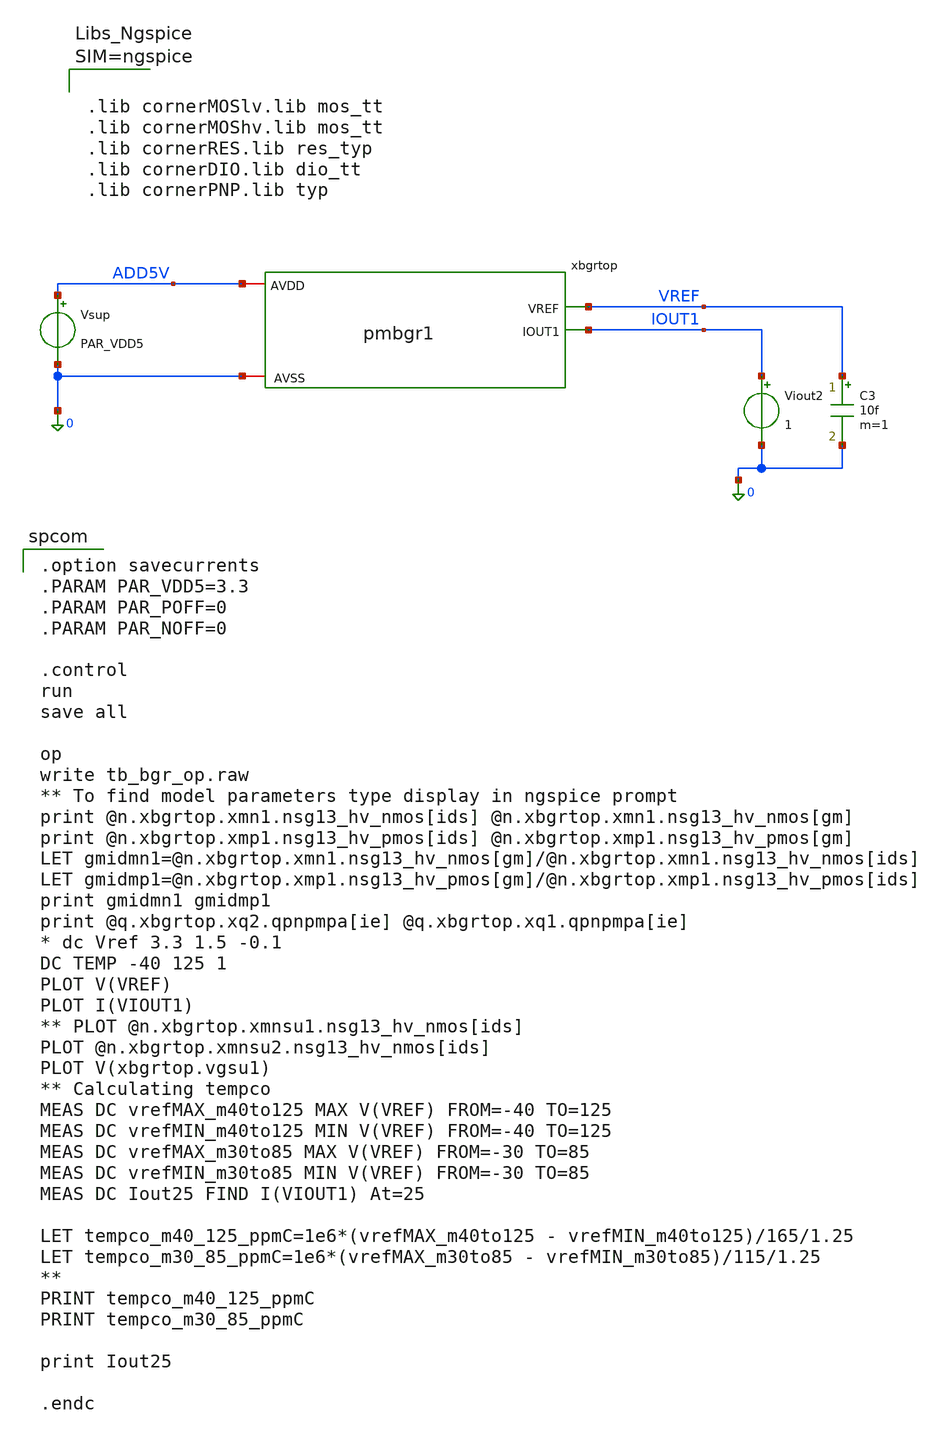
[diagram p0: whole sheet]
** sch_path: xschem/TB_pmbgr1.sch
**.subckt TB_pmbgr1
xbgrtop ADD5V VREF IOUT1 0 pmbgr1
Vsup ADD5V 0 PAR_VDD5
C3 VREF 0 10f m=1
Viout2 IOUT1 0 1
**** begin user architecture code

.option savecurrents
.PARAM PAR_VDD5=3.3
.PARAM PAR_POFF=0
.PARAM PAR_NOFF=0

.control
run
save all

op
write tb_bgr_op.raw
** To find model parameters type display in ngspice prompt
print @n.xbgrtop.xmn1.nsg13_hv_nmos[ids] @n.xbgrtop.xmn1.nsg13_hv_nmos[gm]
print @n.xbgrtop.xmp1.nsg13_hv_pmos[ids] @n.xbgrtop.xmp1.nsg13_hv_pmos[gm]
LET gmidmn1=@n.xbgrtop.xmn1.nsg13_hv_nmos[gm]/@n.xbgrtop.xmn1.nsg13_hv_nmos[ids]
LET gmidmp1=@n.xbgrtop.xmp1.nsg13_hv_pmos[gm]/@n.xbgrtop.xmp1.nsg13_hv_pmos[ids]
print gmidmn1 gmidmp1
print @q.xbgrtop.xq2.qpnpmpa[ie] @q.xbgrtop.xq1.qpnpmpa[ie]
* dc Vref 3.3 1.5 -0.1
DC TEMP -40 125 1
PLOT V(VREF)
PLOT I(VIOUT1)
** PLOT @n.xbgrtop.xmnsu1.nsg13_hv_nmos[ids]
PLOT @n.xbgrtop.xmnsu2.nsg13_hv_nmos[ids]
PLOT V(xbgrtop.vgsu1)
** Calculating tempco
MEAS DC vrefMAX_m40to125 MAX V(VREF) FROM=-40 TO=125
MEAS DC vrefMIN_m40to125 MIN V(VREF) FROM=-40 TO=125
MEAS DC vrefMAX_m30to85 MAX V(VREF) FROM=-30 TO=85
MEAS DC vrefMIN_m30to85 MIN V(VREF) FROM=-30 TO=85
MEAS DC Iout25 FIND I(VIOUT1) At=25

LET tempco_m40_125_ppmC=1e6*(vrefMAX_m40to125 - vrefMIN_m40to125)/165/1.25
LET tempco_m30_85_ppmC=1e6*(vrefMAX_m30to85 - vrefMIN_m30to85)/115/1.25
**
PRINT tempco_m40_125_ppmC
PRINT tempco_m30_85_ppmC

print Iout25

.endc




.lib cornerMOSlv.lib mos_tt
.lib cornerMOShv.lib mos_tt
.lib cornerRES.lib res_typ
.lib cornerDIO.lib dio_tt
.lib cornerPNP.lib typ



**** end user architecture code
**.ends

* expanding   symbol:  pmbgr1.sym # of pins=4
** sym_path: xschem/pmbgr1.sym
** sch_path: xschem/pmbgr1.sch
.subckt pmbgr1 AVDD VREF IOUT1 AVSS
*.iopin AVDD
*.iopin AVSS
*.opin VREF
*.opin IOUT1
XQ1 AVSS AVSS Vbe1 pnpMPA a=2p p=6u m=7
XQ2 AVSS AVSS Vbe2 pnpMPA a=2p p=6u m=1
XMN2 Vgn Vgn Vbe2 AVSS sg13_hv_nmos w=2u l=1u ng=1 m=6 mm_ok=1
XMN1 net1 net2 Vbe2_cp AVSS sg13_hv_nmos w=2u l=1u ng=1 m=12 mm_ok=1
XMP2 Vgn Vgp AVDD AVDD sg13_hv_pmos w=1u l=4u ng=1 m=3 mm_ok=1
XMP1 net1 net1 AVDD AVDD sg13_hv_pmos w=1u l=4u ng=1 m=6 mm_ok=1
XR2 Vbe2_cp Vbe1 AVSS rhigh w=1.1u l=8u m=1 b=0 mm_ok=1
XMP3 IOUT1 net1 AVDD AVDD sg13_hv_pmos w=1u l=4u ng=1 m=6 mm_ok=1
XMP5 VREF Vgp AVDD AVDD sg13_hv_pmos w=1u l=4u ng=1 m=3 mm_ok=1
XR1 VREF Vbe2 AVSS rhigh w=1.1u l=118u m=1 b=0 mm_ok=1
V1 net2 Vgn PAR_NOFF
V2 net1 Vgp PAR_POFF
XMNSU1 AVDD vgsu1 Vgn AVSS sg13_hv_nmos w=1u l=2u ng=1 m=1 mm_ok=1
XMPSU1 net3 VREF AVDD AVDD sg13_hv_pmos w=0.35u l=6u ng=1 m=1 mm_ok=1
XMNSU2 vgsu1 VREF AVSS AVSS sg13_hv_nmos w=2u l=0.5u ng=1 m=1 mm_ok=1
XMPSU2 vgsu1 VREF net3 AVDD sg13_hv_pmos w=0.35u l=6u ng=1 m=1 mm_ok=1
.ends

.end
